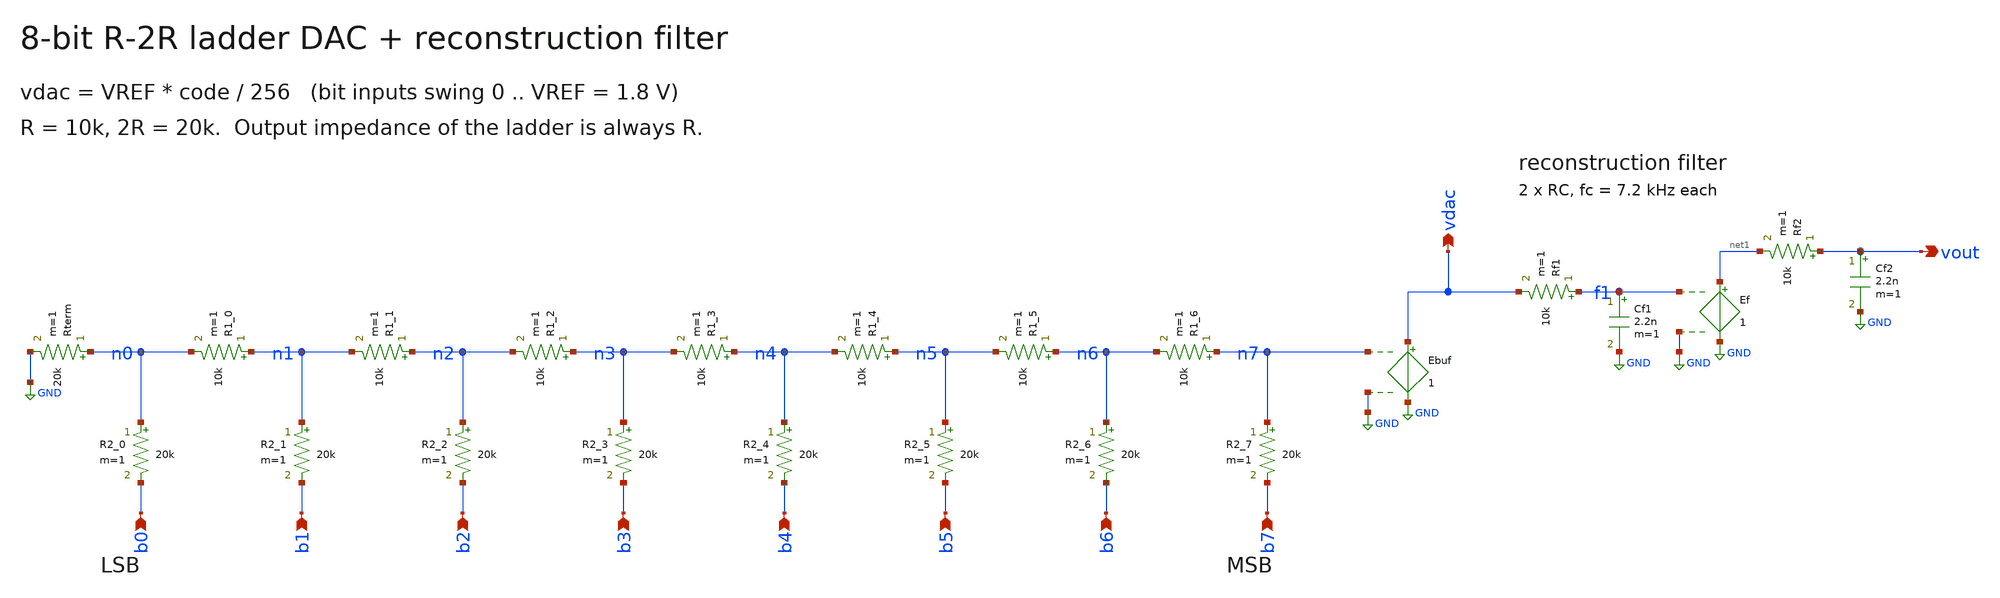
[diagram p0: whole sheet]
** sch_path: analog/sch/dac_r2r8.sch
**.subckt dac_r2r8 b0 b1 b2 b3 b4 b5 b6 b7 vdac vout
*.ipin b0
*.ipin b1
*.ipin b2
*.ipin b3
*.ipin b4
*.ipin b5
*.ipin b6
*.ipin b7
*.opin vdac
*.opin vout
Rterm n0 GND 20k m=1
R2_0 n0 b0 20k m=1
R1_0 n1 n0 10k m=1
R2_1 n1 b1 20k m=1
R1_1 n2 n1 10k m=1
R2_2 n2 b2 20k m=1
R1_2 n3 n2 10k m=1
R2_3 n3 b3 20k m=1
R1_3 n4 n3 10k m=1
R2_4 n4 b4 20k m=1
R1_4 n5 n4 10k m=1
R2_5 n5 b5 20k m=1
R1_5 n6 n5 10k m=1
R2_6 n6 b6 20k m=1
R1_6 n7 n6 10k m=1
R2_7 n7 b7 20k m=1
Ebuf vdac GND n7 GND 1
Rf1 f1 vdac 10k m=1
Cf1 f1 GND 2.2n m=1
Ef net1 GND f1 GND 1
Rf2 vout net1 10k m=1
Cf2 vout GND 2.2n m=1
**.ends
.GLOBAL GND
.end
